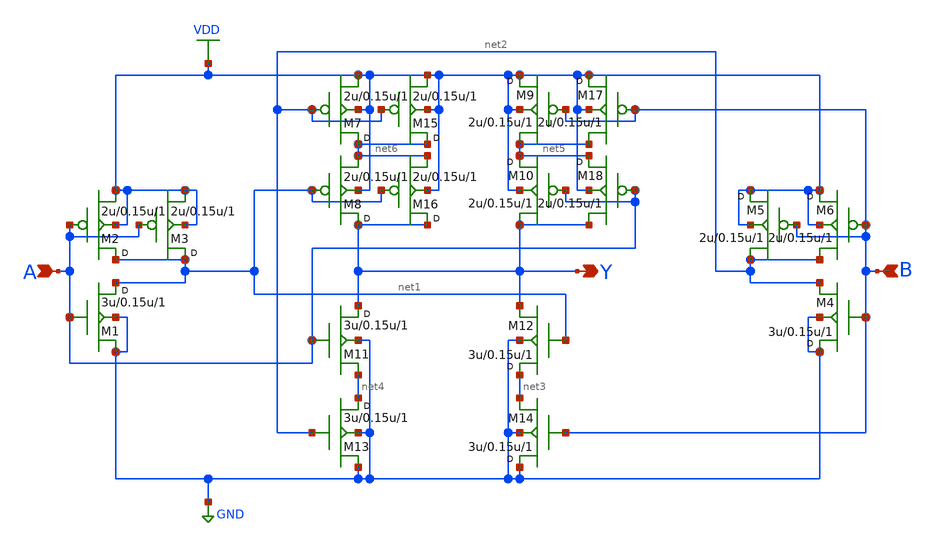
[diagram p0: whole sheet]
** sch_path: lib/xschem/schematics/XNOR2X2.sch
**.subckt XNOR2X2 A Y B
*.ipin A
*.opin Y
*.ipin B
M1 net1 A GND GND nmos w=3u l=0.15u m=1
M2 net1 A VDD VDD pmos w=2u l=0.15u m=1
M3 net1 A VDD VDD pmos w=2u l=0.15u m=1
M4 GND B net2 GND nmos w=3u l=0.15u m=1
M5 VDD B net2 VDD pmos w=2u l=0.15u m=1
M6 VDD B net2 VDD pmos w=2u l=0.15u m=1
M7 net6 net2 VDD VDD pmos w=2u l=0.15u m=1
M8 Y net1 net6 VDD pmos w=2u l=0.15u m=1
M9 VDD B net5 VDD pmos w=2u l=0.15u m=1
M10 net5 A Y VDD pmos w=2u l=0.15u m=1
M11 Y A net4 GND nmos w=3u l=0.15u m=1
M12 net3 net1 Y GND nmos w=3u l=0.15u m=1
M13 net4 net2 GND GND nmos w=3u l=0.15u m=1
M14 GND B net3 GND nmos w=3u l=0.15u m=1
M15 net6 net2 VDD VDD pmos w=2u l=0.15u m=1
M16 Y net1 net6 VDD pmos w=2u l=0.15u m=1
M17 VDD B net5 VDD pmos w=2u l=0.15u m=1
M18 net5 A Y VDD pmos w=2u l=0.15u m=1
**.ends
.GLOBAL VDD
.GLOBAL GND
.end
